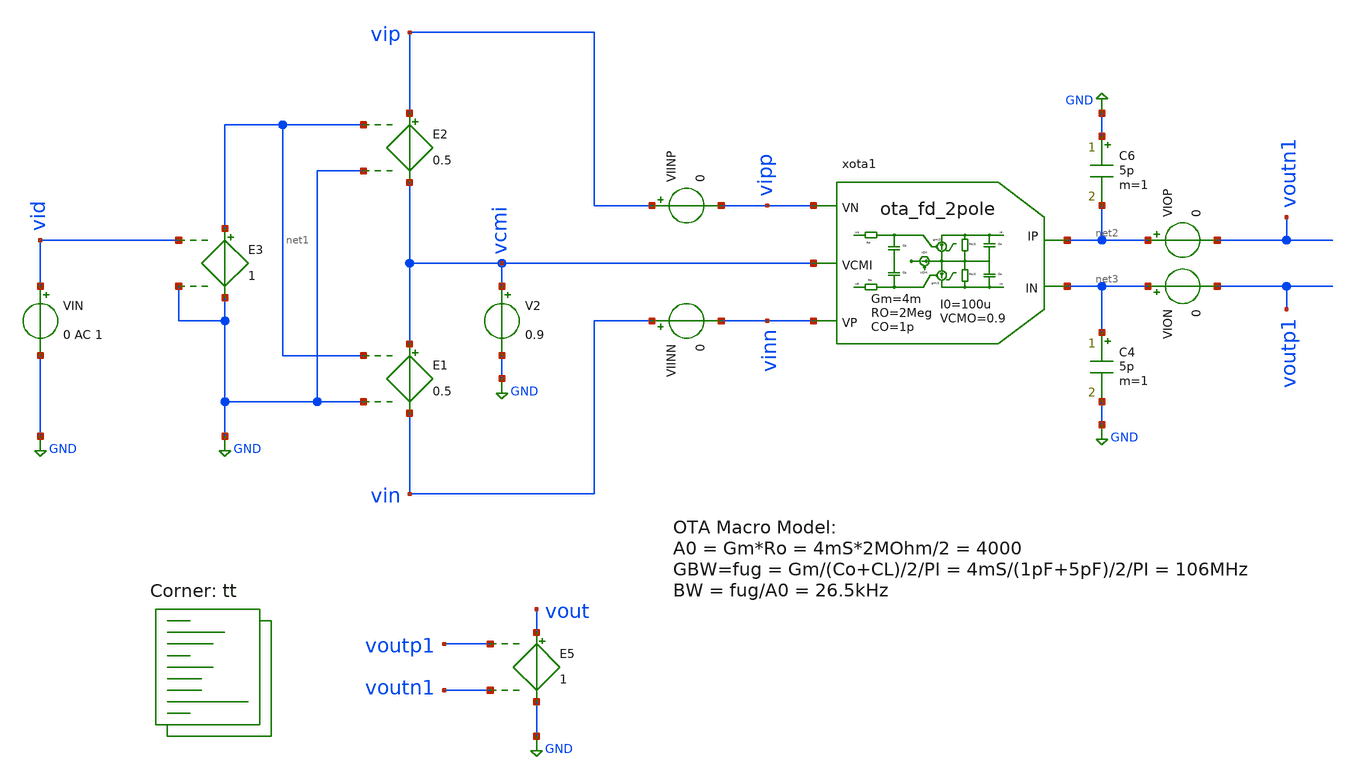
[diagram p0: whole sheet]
** sch_path: xschem/macro-models/tb_ota_fd_2pole.sch
**.subckt tb_ota_fd_2pole
V2 vcmi GND 0.9
E1 vcmi vin net1 GND 0.5
E2 vip vcmi net1 GND 0.5
VIN vid GND 0 AC 1
E3 net1 GND vid GND 1
VIINP vip vipp 0
VIINN vin vinn 0
E5 vout GND voutp1 voutn1 1
VIOP net2 voutn1 0
VION net3 voutp1 0
C4 net3 GND 5p m=1
C6 GND net2 5p m=1
xota1 vipp net2 net3 vinn vcmi ota_fd_2pole GM=4m RO=2Meg CO=1p RP=0 CP=0.1p VCMO=0.9 I0=100u
**** begin user architecture code
.lib $::SKYWATER_MODELS/sky130.lib.spice tt


.options savecurrents
.options method=gear reltol=.005
.options sparse
.control
save all

let f_sig = 100
let f_min = 10
let f_max = 1000Meg
let f_stop = 5Meg
let tper_sig = 1/f_sig
let tfr_sig = tper_sig/2
let Adc = 4000
let v_step_o = 0.9
let v_step_i = v_step_o/Adc

let t_rf = 0.1u
let t_step = 50u
let t_delay = 0
let t_per = 2*t_step

let tstep = 0.1*t_rf
let tstop = 2*t_per
let tstart = t_delay

alter @VIN[PULSE] = [ 0 $&v_step_i $&t_delay $&t_rf $&t_rf $&t_step $&t_per 0 ]

set wr_singlescale
set wr_vecnames
option numdgt=3


** Main Simulations
	op
	ac dec 100 $&const.f_min $&const.f_max
	tran $&tstep $&tstop $&tstart

	setplot ac1
	let A = v(vout)/v(vid)

	let Amag_dB = vdb(A)
	settype decibel Amag_dB
	let Aarg = 180/PI*cphase(A)

	let fdc = const.f_min+1
	meas ac Adc find Amag_dB when frequency = fdc
	let Amag_fc = Adc-3
	meas ac fc find frequency when Amag_dB = Amag_fc
	meas ac Amax max Amag_dB
	meas ac fug find frequency when Amag_dB=0

	let Adc_lin = 10^(Adc/20)
	let GBW = Adc_lin*fc
	print Adc_lin
	print GBW

	plot Amag_dB Aarg ylabel 'Magnitude, Phase'

	setplot tran1
	let vid = v(vid)
	let iop = viop#branch
	let ion = vion#branch
	let vcmo = (voutp1+voutn1)/2

	plot iop ion
	plot vid vout vcmo
	plot v(vip) v(vin) v(voutp1) v(voutn1) vcmo


alter @VIN[DC] = 0
op

remzerovec
write tb_ota_fd_2pole.raw
.endc

**** end user architecture code
**.ends

* expanding   symbol:  /foss/designs/macro-models/ota_fd_2pole.sym # of pins=5
** sym_path: xschem/macro-models/ota_fd_2pole.sym
** sch_path: xschem/macro-models/ota_fd_2pole.sch
.subckt ota_fd_2pole VN IP IN VP VCMI  GM=1u RO=100Meg CO=1p RP=0 CP=0.1p VCMO=0 I0=1u
*.ipin VP
*.ipin VN
*.opin IP
*.opin IN
*.ipin VCMI
R3 IP net1 {{RO}/2} m=1
R4 IN net1 {{RO}/2} m=1
C3 IP net1 {{CO}} m=1
R5 VN ip1 {RP} m=1
C4 ip1 VCMI {CP} m=1
C6 in1 VCMI {CP} m=1
C8 IN net1 {{CO}} m=1
R7 VP in1 {RP} m=1
B2 IP net1 I = {{I0}*tanh({GM}/2*V(ip1,in1)/{I0})}
B1 net1 IN I = {{I0}*tanh({GM}/2*V(ip1,in1)/{I0})}
B5 net1 GND I = {{VCMO}-(V(IP)+V(IN))/2}
.ends

.GLOBAL GND
.end
